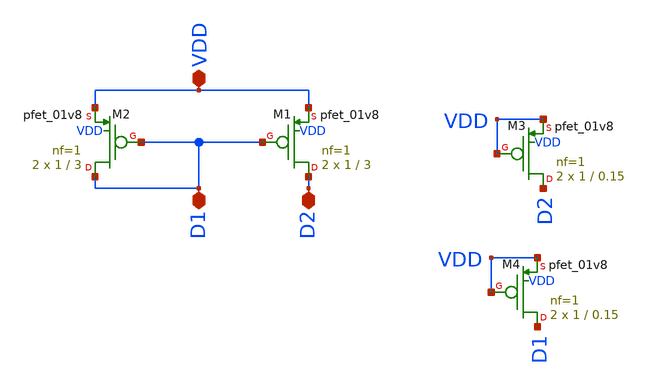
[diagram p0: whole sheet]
** sch_path: magic/pmos_current_source_2.sch
**.subckt pmos_current_source_2 VDD D1 D2
*.iopin VDD
*.iopin D1
*.iopin D2
XM1 D2 D1 VDD VDD sky130_fd_pr__pfet_01v8 L=3 W=1 nf=1 ad='int((nf+1)/2) * W/nf * 0.29' as='int((nf+2)/2) * W/nf * 0.29'
+ pd='2*int((nf+1)/2) * (W/nf + 0.29)' ps='2*int((nf+2)/2) * (W/nf + 0.29)' nrd='0.29 / W' nrs='0.29 / W'
+ sa=0 sb=0 sd=0 mult=2 m=2
XM2 D1 D1 VDD VDD sky130_fd_pr__pfet_01v8 L=3 W=1 nf=1 ad='int((nf+1)/2) * W/nf * 0.29' as='int((nf+2)/2) * W/nf * 0.29'
+ pd='2*int((nf+1)/2) * (W/nf + 0.29)' ps='2*int((nf+2)/2) * (W/nf + 0.29)' nrd='0.29 / W' nrs='0.29 / W'
+ sa=0 sb=0 sd=0 mult=2 m=2
XM3 D2 VDD VDD VDD sky130_fd_pr__pfet_01v8 L=0.15 W=1 nf=1 ad='int((nf+1)/2) * W/nf * 0.29' as='int((nf+2)/2) * W/nf * 0.29'
+ pd='2*int((nf+1)/2) * (W/nf + 0.29)' ps='2*int((nf+2)/2) * (W/nf + 0.29)' nrd='0.29 / W' nrs='0.29 / W'
+ sa=0 sb=0 sd=0 mult=2 m=2
XM4 D1 VDD VDD VDD sky130_fd_pr__pfet_01v8 L=0.15 W=1 nf=1 ad='int((nf+1)/2) * W/nf * 0.29' as='int((nf+2)/2) * W/nf * 0.29'
+ pd='2*int((nf+1)/2) * (W/nf + 0.29)' ps='2*int((nf+2)/2) * (W/nf + 0.29)' nrd='0.29 / W' nrs='0.29 / W'
+ sa=0 sb=0 sd=0 mult=2 m=2
**.ends
.end
